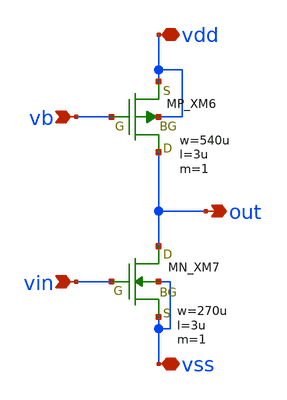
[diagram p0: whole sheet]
** sch_path: member_project/OPAMP/ShuntaroOhno/xschem/cs.sch
**.subckt cs vb vin out vss vdd
*.ipin vb
*.ipin vin
*.opin out
*.iopin vss
*.iopin vdd
XM6 out vb vdd vdd PMOS w=540u l=3u as=0 ad=0 ps=0 pd=0 nrd=0 nrs=0 m=1
XM7 out vin vss vss NMOS w=270u l=3u as=0 ad=0 ps=0 pd=0 nrd=0 nrs=0 m=1
**.ends
.end
